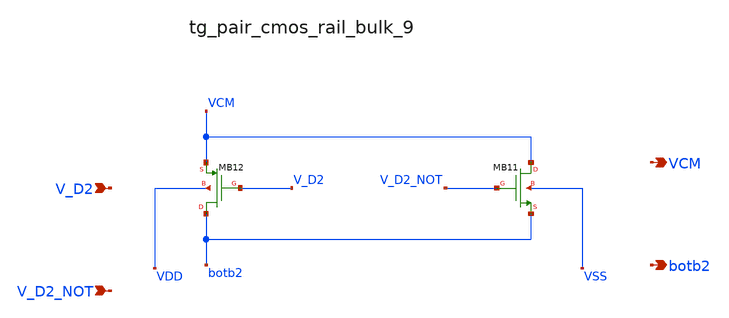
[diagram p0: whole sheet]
** sch_path: analog-db/raw/ia_005_hsu_pga_ideal/hier/blocks/tg_pair_cmos_rail_bulk_9.sch
**.subckt tg_pair_cmos_rail_bulk_9 V_D2 V_D2_NOT VCM botb2
*.ipin V_D2
*.ipin V_D2_NOT
*.opin VCM
*.opin botb2
XMB11 VCM V_D2_NOT botb2 VSS sg13_lv_nmos w=x_dut_xmb11_w l=x_dut_xmb11_l ng=1 m=x_dut_xmb11_m
XMB12 botb2 V_D2 VCM VDD sg13_lv_pmos w=x_dut_xmb12_w l=x_dut_xmb12_l ng=1 m=x_dut_xmb12_m
**.ends
.end
